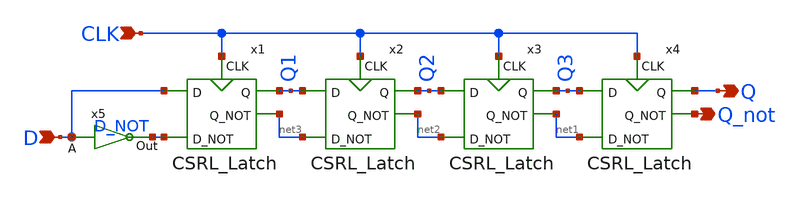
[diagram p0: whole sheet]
** sch_path: miniproject2/4BIT_SHIFT_REGISTER.sch
**.subckt 4BIT_SHIFT_REGISTER Q Q_not D CLK
*.opin Q
*.opin Q_not
*.ipin D
*.ipin CLK
x1 D Q1 D_NOT net3 CLK CSRL_Latch
x2 Q1 Q2 net3 net2 CLK CSRL_Latch
x3 Q2 Q3 net2 net1 CLK CSRL_Latch
x4 Q3 Q net1 Q_not CLK CSRL_Latch
x5 D_NOT D MP1_inverter
**.ends

* expanding   symbol:  /home/lxbtlr/MAD/miniproject2/CSRL_Latch.sym # of pins=5
** sym_path: miniproject2/CSRL_Latch.sym
** sch_path: miniproject2/CSRL_Latch.sch
.subckt CSRL_Latch D Q D_NOT Q_NOT CLK
*.ipin D
*.ipin D_NOT
*.opin Q
*.opin Q_NOT
*.ipin CLK
XQ8 net1 net2 VDD VDD sky130_fd_pr__pfet_01v8 L=0.15 W=1 nf=1 ad='int((nf+1)/2) * W/nf * 0.29' as='int((nf+2)/2) * W/nf * 0.29'
+ pd='2*int((nf+1)/2) * (W/nf + 0.29)' ps='2*int((nf+2)/2) * (W/nf + 0.29)' nrd='0.29 / W' nrs='0.29 / W'
+ sa=0 sb=0 sd=0 mult=1 m=1
XQ9 VDD net1 net2 VDD sky130_fd_pr__pfet_01v8 L=0.15 W=1 nf=1 ad='int((nf+1)/2) * W/nf * 0.29' as='int((nf+2)/2) * W/nf * 0.29'
+ pd='2*int((nf+1)/2) * (W/nf + 0.29)' ps='2*int((nf+2)/2) * (W/nf + 0.29)' nrd='0.29 / W' nrs='0.29 / W'
+ sa=0 sb=0 sd=0 mult=1 m=1
XQ1 net2 CLK D VDD sky130_fd_pr__pfet_01v8 L=0.15 W=1 nf=1 ad='int((nf+1)/2) * W/nf * 0.29' as='int((nf+2)/2) * W/nf * 0.29'
+ pd='2*int((nf+1)/2) * (W/nf + 0.29)' ps='2*int((nf+2)/2) * (W/nf + 0.29)' nrd='0.29 / W' nrs='0.29 / W'
+ sa=0 sb=0 sd=0 mult=1 m=1
XQ2 net1 CLK D_NOT VDD sky130_fd_pr__pfet_01v8 L=0.15 W=1 nf=1 ad='int((nf+1)/2) * W/nf * 0.29' as='int((nf+2)/2) * W/nf * 0.29'
+ pd='2*int((nf+1)/2) * (W/nf + 0.29)' ps='2*int((nf+2)/2) * (W/nf + 0.29)' nrd='0.29 / W' nrs='0.29 / W'
+ sa=0 sb=0 sd=0 mult=1 m=1
XQ5 net4 CLK GND GND sky130_fd_pr__nfet_01v8 L=0.15 W=4 nf=1 ad='int((nf+1)/2) * W/nf * 0.29' as='int((nf+2)/2) * W/nf * 0.29'
+ pd='2*int((nf+1)/2) * (W/nf + 0.29)' ps='2*int((nf+2)/2) * (W/nf + 0.29)' nrd='0.29 / W' nrs='0.29 / W'
+ sa=0 sb=0 sd=0 mult=1 m=1
XQ4 Q_NOT CLK net1 GND sky130_fd_pr__nfet_01v8 L=0.15 W=1 nf=1 ad='int((nf+1)/2) * W/nf * 0.29' as='int((nf+2)/2) * W/nf * 0.29'
+ pd='2*int((nf+1)/2) * (W/nf + 0.29)' ps='2*int((nf+2)/2) * (W/nf + 0.29)' nrd='0.29 / W' nrs='0.29 / W'
+ sa=0 sb=0 sd=0 mult=1 m=1
XQ3 Q CLK net2 GND sky130_fd_pr__nfet_01v8 L=0.15 W=1 nf=1 ad='int((nf+1)/2) * W/nf * 0.29' as='int((nf+2)/2) * W/nf * 0.29'
+ pd='2*int((nf+1)/2) * (W/nf + 0.29)' ps='2*int((nf+2)/2) * (W/nf + 0.29)' nrd='0.29 / W' nrs='0.29 / W'
+ sa=0 sb=0 sd=0 mult=1 m=1
XQ6 net1 net2 net4 GND sky130_fd_pr__nfet_01v8 L=0.15 W=1 nf=1 ad='int((nf+1)/2) * W/nf * 0.29' as='int((nf+2)/2) * W/nf * 0.29'
+ pd='2*int((nf+1)/2) * (W/nf + 0.29)' ps='2*int((nf+2)/2) * (W/nf + 0.29)' nrd='0.29 / W' nrs='0.29 / W'
+ sa=0 sb=0 sd=0 mult=1 m=1
XQ7 net4 net1 net2 GND sky130_fd_pr__nfet_01v8 L=0.15 W=1 nf=1 ad='int((nf+1)/2) * W/nf * 0.29' as='int((nf+2)/2) * W/nf * 0.29'
+ pd='2*int((nf+1)/2) * (W/nf + 0.29)' ps='2*int((nf+2)/2) * (W/nf + 0.29)' nrd='0.29 / W' nrs='0.29 / W'
+ sa=0 sb=0 sd=0 mult=1 m=1
XQ13 Q_NOT Q GND GND sky130_fd_pr__nfet_01v8 L=0.15 W=1 nf=1 ad='int((nf+1)/2) * W/nf * 0.29' as='int((nf+2)/2) * W/nf * 0.29'
+ pd='2*int((nf+1)/2) * (W/nf + 0.29)' ps='2*int((nf+2)/2) * (W/nf + 0.29)' nrd='0.29 / W' nrs='0.29 / W'
+ sa=0 sb=0 sd=0 mult=1 m=1
XQ14 GND Q_NOT Q GND sky130_fd_pr__nfet_01v8 L=0.15 W=1 nf=1 ad='int((nf+1)/2) * W/nf * 0.29' as='int((nf+2)/2) * W/nf * 0.29'
+ pd='2*int((nf+1)/2) * (W/nf + 0.29)' ps='2*int((nf+2)/2) * (W/nf + 0.29)' nrd='0.29 / W' nrs='0.29 / W'
+ sa=0 sb=0 sd=0 mult=1 m=1
XQ11 Q_NOT Q net3 VDD sky130_fd_pr__pfet_01v8 L=0.15 W=1 nf=1 ad='int((nf+1)/2) * W/nf * 0.29' as='int((nf+2)/2) * W/nf * 0.29'
+ pd='2*int((nf+1)/2) * (W/nf + 0.29)' ps='2*int((nf+2)/2) * (W/nf + 0.29)' nrd='0.29 / W' nrs='0.29 / W'
+ sa=0 sb=0 sd=0 mult=1 m=1
XQ12 net3 Q_NOT Q VDD sky130_fd_pr__pfet_01v8 L=0.15 W=1 nf=1 ad='int((nf+1)/2) * W/nf * 0.29' as='int((nf+2)/2) * W/nf * 0.29'
+ pd='2*int((nf+1)/2) * (W/nf + 0.29)' ps='2*int((nf+2)/2) * (W/nf + 0.29)' nrd='0.29 / W' nrs='0.29 / W'
+ sa=0 sb=0 sd=0 mult=1 m=1
XQ10 net3 CLK VDD VDD sky130_fd_pr__pfet_01v8 L=0.15 W=4 nf=1 ad='int((nf+1)/2) * W/nf * 0.29' as='int((nf+2)/2) * W/nf * 0.29'
+ pd='2*int((nf+1)/2) * (W/nf + 0.29)' ps='2*int((nf+2)/2) * (W/nf + 0.29)' nrd='0.29 / W' nrs='0.29 / W'
+ sa=0 sb=0 sd=0 mult=1 m=1
.ends


* expanding   symbol:  /home/lxbtlr/MAD/miniproject1/MP1_inverter.sym # of pins=2
** sym_path: miniproject2/MP1_inverter.sym
** sch_path: miniproject2/MP1_inverter.sch
.subckt MP1_inverter Out A
*.ipin A
*.opin Out
XM1 Out A VDD VDD sky130_fd_pr__pfet_01v8 L=0.15 W=1 nf=1 ad='int((nf+1)/2) * W/nf * 0.29' as='int((nf+2)/2) * W/nf * 0.29'
+ pd='2*int((nf+1)/2) * (W/nf + 0.29)' ps='2*int((nf+2)/2) * (W/nf + 0.29)' nrd='0.29 / W' nrs='0.29 / W'
+ sa=0 sb=0 sd=0 mult=1 m=1
XM2 Out A GND GND sky130_fd_pr__nfet_01v8 L=0.15 W=1 nf=1 ad='int((nf+1)/2) * W/nf * 0.29' as='int((nf+2)/2) * W/nf * 0.29'
+ pd='2*int((nf+1)/2) * (W/nf + 0.29)' ps='2*int((nf+2)/2) * (W/nf + 0.29)' nrd='0.29 / W' nrs='0.29 / W'
+ sa=0 sb=0 sd=0 mult=1 m=1
.ends

.GLOBAL GND
.GLOBAL VDD
.end
